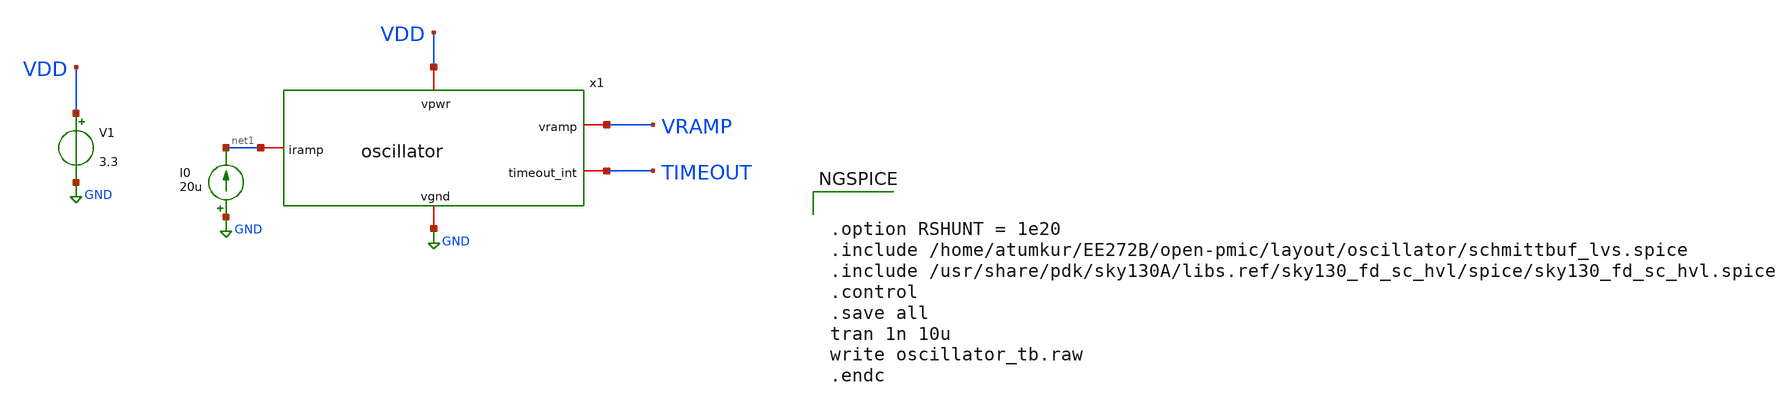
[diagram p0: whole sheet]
** sch_path: images/iic-osic-tools/addons/examples/open-pmic/design/oscillator/oscillator_tb.sch
**.subckt oscillator_tb
x1 net1 TIMEOUT VDD VRAMP GND oscillator
V1 VDD GND 3.3
I0 GND net1 20u
**** begin user architecture code

.include $::SKYWATER_MODELS/cells/nfet_01v8/sky130_fd_pr__nfet_01v8__tt.corner.spice
.include $::SKYWATER_MODELS/cells/nfet_01v8_lvt/sky130_fd_pr__nfet_01v8_lvt__tt.corner.spice
.include $::SKYWATER_MODELS/cells/pfet_01v8/sky130_fd_pr__pfet_01v8__tt.corner.spice
.include $::SKYWATER_MODELS/cells/nfet_03v3_nvt/sky130_fd_pr__nfet_03v3_nvt__tt.corner.spice
.include $::SKYWATER_MODELS/cells/nfet_05v0_nvt/sky130_fd_pr__nfet_05v0_nvt__tt.corner.spice
.include $::SKYWATER_MODELS/cells/esd_nfet_01v8/sky130_fd_pr__esd_nfet_01v8__tt.corner.spice
.include $::SKYWATER_MODELS/cells/pfet_01v8_lvt/sky130_fd_pr__pfet_01v8_lvt__tt.corner.spice
.include $::SKYWATER_MODELS/cells/pfet_01v8_hvt/sky130_fd_pr__pfet_01v8_hvt__tt.corner.spice
.include $::SKYWATER_MODELS/cells/esd_pfet_g5v0d10v5/sky130_fd_pr__esd_pfet_g5v0d10v5__tt.corner.spice
.include $::SKYWATER_MODELS/cells/pfet_g5v0d10v5/sky130_fd_pr__pfet_g5v0d10v5__tt.corner.spice
.include $::SKYWATER_MODELS/cells/pfet_g5v0d16v0/sky130_fd_pr__pfet_g5v0d16v0__tt.corner.spice
.include $::SKYWATER_MODELS/cells/nfet_g5v0d10v5/sky130_fd_pr__nfet_g5v0d10v5__tt.corner.spice
.include $::SKYWATER_MODELS/cells/nfet_g5v0d16v0/sky130_fd_pr__nfet_g5v0d16v0__tt_discrete.corner.spice
.include $::SKYWATER_MODELS/cells/esd_nfet_g5v0d10v5/sky130_fd_pr__esd_nfet_g5v0d10v5__tt.corner.spice
.include $::SKYWATER_MODELS/models/corners/tt/nonfet.spice
* Mismatch parameters
.include $::SKYWATER_MODELS/cells/nfet_01v8/sky130_fd_pr__nfet_01v8__mismatch.corner.spice
.include $::SKYWATER_MODELS/cells/pfet_01v8/sky130_fd_pr__pfet_01v8__mismatch.corner.spice
.include $::SKYWATER_MODELS/cells/nfet_01v8_lvt/sky130_fd_pr__nfet_01v8_lvt__mismatch.corner.spice
.include $::SKYWATER_MODELS/cells/pfet_01v8_lvt/sky130_fd_pr__pfet_01v8_lvt__mismatch.corner.spice
.include $::SKYWATER_MODELS/cells/pfet_01v8_hvt/sky130_fd_pr__pfet_01v8_hvt__mismatch.corner.spice
.include $::SKYWATER_MODELS/cells/nfet_g5v0d10v5/sky130_fd_pr__nfet_g5v0d10v5__mismatch.corner.spice
.include $::SKYWATER_MODELS/cells/pfet_g5v0d10v5/sky130_fd_pr__pfet_g5v0d10v5__mismatch.corner.spice
.include $::SKYWATER_MODELS/cells/nfet_05v0_nvt/sky130_fd_pr__nfet_05v0_nvt__mismatch.corner.spice
.include $::SKYWATER_MODELS/cells/nfet_03v3_nvt/sky130_fd_pr__nfet_03v3_nvt__mismatch.corner.spice
* Resistor$::SKYWATER_MODELS/Capacitor
.include $::SKYWATER_MODELS/models/r+c/res_typical__cap_typical.spice
.include $::SKYWATER_MODELS/models/r+c/res_typical__cap_typical__lin.spice
* Special cells
.include $::SKYWATER_MODELS/models/corners/tt/specialized_cells.spice
* All models
.include $::SKYWATER_MODELS/models/all.spice
* Corner
.include $::SKYWATER_MODELS/models/corners/tt/rf.spice



.option RSHUNT = 1e20
.include /home/atumkur/EE272B/open-pmic/layout/oscillator/schmittbuf_lvs.spice
.include /usr/share/pdk/sky130A/libs.ref/sky130_fd_sc_hvl/spice/sky130_fd_sc_hvl.spice
.control
.save all
tran 1n 10u
write oscillator_tb.raw
.endc


**** end user architecture code
**.ends
.GLOBAL GND
**** begin user architecture code
[sky130_models]
**** end user architecture code
.end
